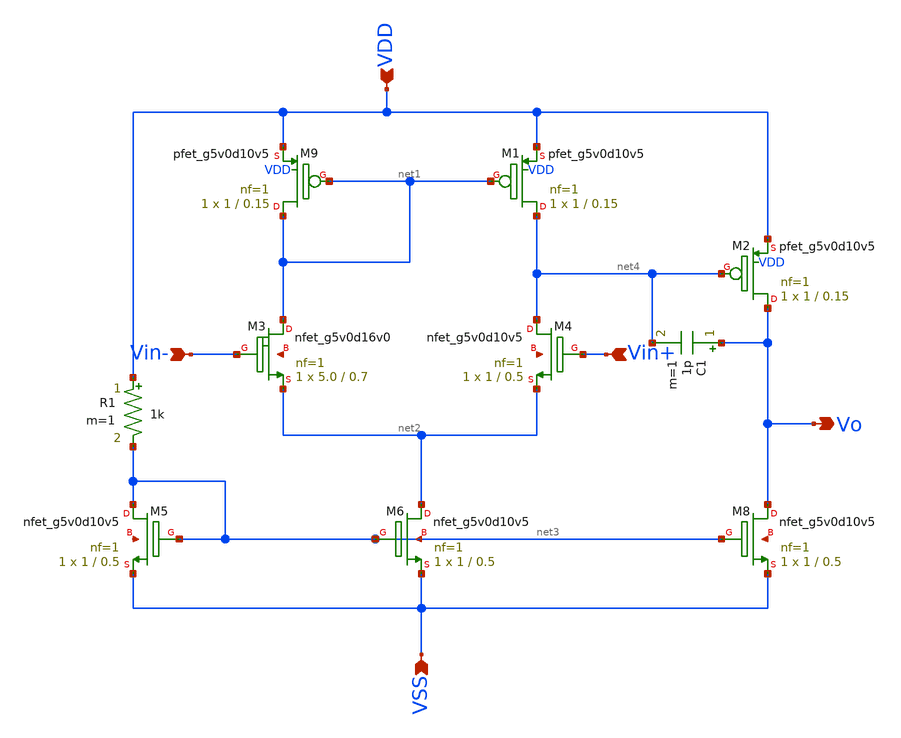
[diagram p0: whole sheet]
** sch_path: hw01/xschem/hw01.sch
**.subckt hw01 VDD Vin- Vin+ VSS Vo
*.ipin VDD
*.ipin Vin-
*.ipin Vin+
*.ipin VSS
*.opin Vo
XM4 net4 Vin+ net2 net5 sky130_fd_pr__nfet_g5v0d10v5 L=0.5 W=1 nf=1 ad='int((nf+1)/2) * W/nf * 0.29'
+ as='int((nf+2)/2) * W/nf * 0.29' pd='2*int((nf+1)/2) * (W/nf + 0.29)' ps='2*int((nf+2)/2) * (W/nf + 0.29)'
+ nrd='0.29 / W' nrs='0.29 / W' sa=0 sb=0 sd=0 mult=1 m=1
XM5 net3 net3 VSS net6 sky130_fd_pr__nfet_g5v0d10v5 L=0.5 W=1 nf=1 ad='int((nf+1)/2) * W/nf * 0.29' as='int((nf+2)/2) * W/nf * 0.29'
+ pd='2*int((nf+1)/2) * (W/nf + 0.29)' ps='2*int((nf+2)/2) * (W/nf + 0.29)' nrd='0.29 / W' nrs='0.29 / W'
+ sa=0 sb=0 sd=0 mult=1 m=1
XM6 net2 net3 VSS net3 sky130_fd_pr__nfet_g5v0d10v5 L=0.5 W=1 nf=1 ad='int((nf+1)/2) * W/nf * 0.29' as='int((nf+2)/2) * W/nf * 0.29'
+ pd='2*int((nf+1)/2) * (W/nf + 0.29)' ps='2*int((nf+2)/2) * (W/nf + 0.29)' nrd='0.29 / W' nrs='0.29 / W'
+ sa=0 sb=0 sd=0 mult=1 m=1
XM8 Vo net3 VSS net7 sky130_fd_pr__nfet_g5v0d10v5 L=0.5 W=1 nf=1 ad='int((nf+1)/2) * W/nf * 0.29' as='int((nf+2)/2) * W/nf * 0.29'
+ pd='2*int((nf+1)/2) * (W/nf + 0.29)' ps='2*int((nf+2)/2) * (W/nf + 0.29)' nrd='0.29 / W' nrs='0.29 / W'
+ sa=0 sb=0 sd=0 mult=1 m=1
R1 VDD net3 1k m=1
C1 Vo net4 1p m=1
XM9 net1 net1 VDD VDD sky130_fd_pr__pfet_g5v0d10v5 L=0.15 W=1 nf=1 ad='int((nf+1)/2) * W/nf * 0.29' as='int((nf+2)/2) * W/nf * 0.29'
+ pd='2*int((nf+1)/2) * (W/nf + 0.29)' ps='2*int((nf+2)/2) * (W/nf + 0.29)' nrd='0.29 / W' nrs='0.29 / W'
+ sa=0 sb=0 sd=0 mult=1 m=1
XM1 net4 net1 VDD VDD sky130_fd_pr__pfet_g5v0d10v5 L=0.15 W=1 nf=1 ad='int((nf+1)/2) * W/nf * 0.29' as='int((nf+2)/2) * W/nf * 0.29'
+ pd='2*int((nf+1)/2) * (W/nf + 0.29)' ps='2*int((nf+2)/2) * (W/nf + 0.29)' nrd='0.29 / W' nrs='0.29 / W'
+ sa=0 sb=0 sd=0 mult=1 m=1
XM2 Vo net4 VDD VDD sky130_fd_pr__pfet_g5v0d10v5 L=0.15 W=1 nf=1 ad='int((nf+1)/2) * W/nf * 0.29' as='int((nf+2)/2) * W/nf * 0.29'
+ pd='2*int((nf+1)/2) * (W/nf + 0.29)' ps='2*int((nf+2)/2) * (W/nf + 0.29)' nrd='0.29 / W' nrs='0.29 / W'
+ sa=0 sb=0 sd=0 mult=1 m=1
XM3 net1 Vin- net2 net8 sky130_fd_pr__nfet_g5v0d16v0 L=0.7 W=5.0 nf=1 ad='int((nf+1)/2) * W/nf * 0.29'
+ as='int((nf+2)/2) * W/nf * 0.29' pd='2*int((nf+1)/2) * (W/nf + 0.29)' ps='2*int((nf+2)/2) * (W/nf + 0.29)'
+ nrd='0.29 / W' nrs='0.29 / W' sa=0 sb=0 sd=0 mult=1 m=1
**.ends
.end
